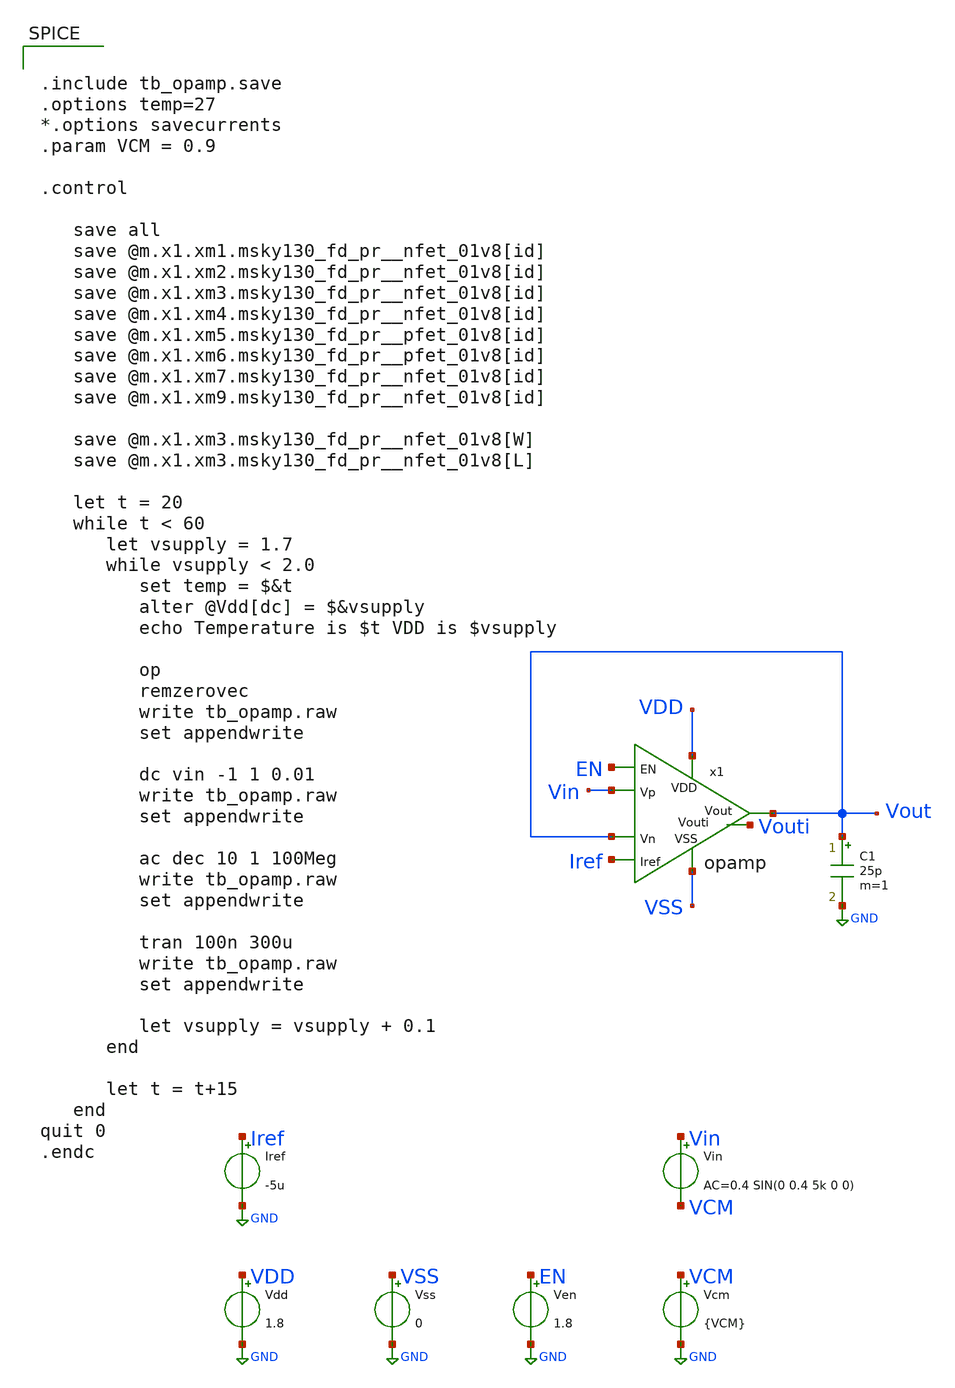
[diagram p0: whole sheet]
** sch_path: xschem/tb_closed_opamp.sch
**.subckt tb_closed_opamp
Vdd VDD GND 1.8
Vss VSS GND 0
Vin Vin VCM AC=0.4 SIN(0 0.4 5k 0 0)
Iref Iref GND -5u
x1 Vout Vout Vin VSS Iref VDD Vouti EN opamp
Ven EN GND 1.8
C1 Vout GND 25p m=1
Vcm VCM GND {VCM}
**** begin user architecture code


.include tb_opamp.save
.options temp=27
*.options savecurrents
.param VCM = 0.9

.control

   save all
   save @m.x1.xm1.msky130_fd_pr__nfet_01v8[id]
   save @m.x1.xm2.msky130_fd_pr__nfet_01v8[id]
   save @m.x1.xm3.msky130_fd_pr__nfet_01v8[id]
   save @m.x1.xm4.msky130_fd_pr__nfet_01v8[id]
   save @m.x1.xm5.msky130_fd_pr__pfet_01v8[id]
   save @m.x1.xm6.msky130_fd_pr__pfet_01v8[id]
   save @m.x1.xm7.msky130_fd_pr__nfet_01v8[id]
   save @m.x1.xm9.msky130_fd_pr__nfet_01v8[id]

   save @m.x1.xm3.msky130_fd_pr__nfet_01v8[W]
   save @m.x1.xm3.msky130_fd_pr__nfet_01v8[L]

   let t = 20
   while t < 60
      let vsupply = 1.7
      while vsupply < 2.0
         set temp = $&t
         alter @Vdd[dc] = $&vsupply
         echo Temperature is $t VDD is $vsupply

         op
         remzerovec
         write tb_opamp.raw
         set appendwrite

         dc vin -1 1 0.01
         write tb_opamp.raw
         set appendwrite

         ac dec 10 1 100Meg
         write tb_opamp.raw
         set appendwrite

         tran 100n 300u
         write tb_opamp.raw
         set appendwrite

         let vsupply = vsupply + 0.1
      end

      let t = t+15
   end
quit 0
.endc



** opencircuitdesign pdks install
.param MT_SWITCH = 1.0
.lib $::SKYWATER_MODELS/sky130.lib.spice tt

**** end user architecture code
**.ends

* expanding   symbol:  /foss/designs/ttsky_opamp/xschem/opamp.sym # of pins=8
** sym_path: xschem/opamp.sym
** sch_path: xschem/opamp.sch
.subckt opamp Vout Vn Vp VSS Iref VDD Vouti EN
*.ipin VSS
*.ipin Vp
*.opin Vout
*.ipin Vn
*.ipin VDD
*.ipin Iref
*.opin Vouti
*.ipin EN
XM1 VGref VGref VSS VSS sky130_fd_pr__nfet_01v8 L=0.5 W=4 nf=1 ad='int((1 + 1)/2) * 4 / 1 * 0.29' as='int((1 + 2)/2) * 4 / 1 * 0.29'
+ pd='2*int((1 + 1)/2) * (4 / 1 + 0.29)' ps='2*int((1 + 2)/2) * (4 / 1 + 0.29)' nrd='0.29 / 4 ' nrs='0.29 / 4 '
+ sa=0 sb=0 sd=0 mult=1 m=1
XM2 Vx VGref VSS VSS sky130_fd_pr__nfet_01v8 L=0.5 W=4 nf=1 ad='int((1 + 1)/2) * 4 / 1 * 0.29' as='int((1 + 2)/2) * 4 / 1 * 0.29'
+ pd='2*int((1 + 1)/2) * (4 / 1 + 0.29)' ps='2*int((1 + 2)/2) * (4 / 1 + 0.29)' nrd='0.29 / 4 ' nrs='0.29 / 4 '
+ sa=0 sb=0 sd=0 mult=1 m=1
XM3 Vouti Vp Vx VSS sky130_fd_pr__nfet_01v8 L=4 W=10 nf=1 ad='int((1 + 1)/2) * 10 / 1 * 0.29' as='int((1 + 2)/2) * 10 / 1 * 0.29'
+ pd='2*int((1 + 1)/2) * (10 / 1 + 0.29)' ps='2*int((1 + 2)/2) * (10 / 1 + 0.29)' nrd='0.29 / 10 ' nrs='0.29 / 10 '
+ sa=0 sb=0 sd=0 mult=1 m=1
XM4 Vg2 Vn Vx VSS sky130_fd_pr__nfet_01v8 L=4 W=10 nf=1 ad='int((1 + 1)/2) * 10 / 1 * 0.29' as='int((1 + 2)/2) * 10 / 1 * 0.29'
+ pd='2*int((1 + 1)/2) * (10 / 1 + 0.29)' ps='2*int((1 + 2)/2) * (10 / 1 + 0.29)' nrd='0.29 / 10 ' nrs='0.29 / 10 '
+ sa=0 sb=0 sd=0 mult=1 m=1
XM5 Vouti Vg2 VDD VDD sky130_fd_pr__pfet_01v8 L=4.0 W=10.5 nf=1 ad='int((1 + 1)/2) * 10.5 / 1 * 0.29'
+ as='int((1 + 2)/2) * 10.5 / 1 * 0.29' pd='2*int((1 + 1)/2) * (10.5 / 1 + 0.29)' ps='2*int((1 + 2)/2) * (10.5 / 1 + 0.29)'
+ nrd='0.29 / 10.5 ' nrs='0.29 / 10.5 ' sa=0 sb=0 sd=0 mult=1 m=1
XM6 Vg2 Vg2 VDD VDD sky130_fd_pr__pfet_01v8 L=4.0 W=10.5 nf=1 ad='int((1 + 1)/2) * 10.5 / 1 * 0.29' as='int((1 + 2)/2) * 10.5 / 1 * 0.29'
+ pd='2*int((1 + 1)/2) * (10.5 / 1 + 0.29)' ps='2*int((1 + 2)/2) * (10.5 / 1 + 0.29)' nrd='0.29 / 10.5 '
+ nrs='0.29 / 10.5 ' sa=0 sb=0 sd=0 mult=1 m=1
XM7 Vout VGref VSS VSS sky130_fd_pr__nfet_01v8 L=0.5 W=48 nf=8 ad='int((8 + 1)/2) * 48 / 8 * 0.29' as='int((8 + 2)/2) * 48 / 8 * 0.29'
+ pd='2*int((8 + 1)/2) * (48 / 8 + 0.29)' ps='2*int((8 + 2)/2) * (48 / 8 + 0.29)' nrd='0.29 / 48 ' nrs='0.29 / 48 '
+ sa=0 sb=0 sd=0 mult=1 m=1
XM8 Vout Vouti VDD VDD sky130_fd_pr__pfet_01v8 L=0.5 W=20 nf=2 ad='int((2 + 1)/2) * 20 / 2 * 0.29' as='int((2 + 2)/2) * 20 / 2 * 0.29'
+ pd='2*int((2 + 1)/2) * (20 / 2 + 0.29)' ps='2*int((2 + 2)/2) * (20 / 2 + 0.29)' nrd='0.29 / 20 ' nrs='0.29 / 20 '
+ sa=0 sb=0 sd=0 mult=1 m=1
XM9 Iref EN VGref VSS sky130_fd_pr__nfet_01v8 L=2 W=2 nf=1 ad='int((1 + 1)/2) * 2 / 1 * 0.29' as='int((1 + 2)/2) * 2 / 1 * 0.29'
+ pd='2*int((1 + 1)/2) * (2 / 1 + 0.29)' ps='2*int((1 + 2)/2) * (2 / 1 + 0.29)' nrd='0.29 / 2 ' nrs='0.29 / 2 '
+ sa=0 sb=0 sd=0 mult=1 m=1
R1 Vout net1 10k m=1
XC1 Vouti net1 sky130_fd_pr__cap_mim_m3_1 W=40 L=40 MF=1 m=1
.ends

.GLOBAL GND
.GLOBAL VDD
.end
